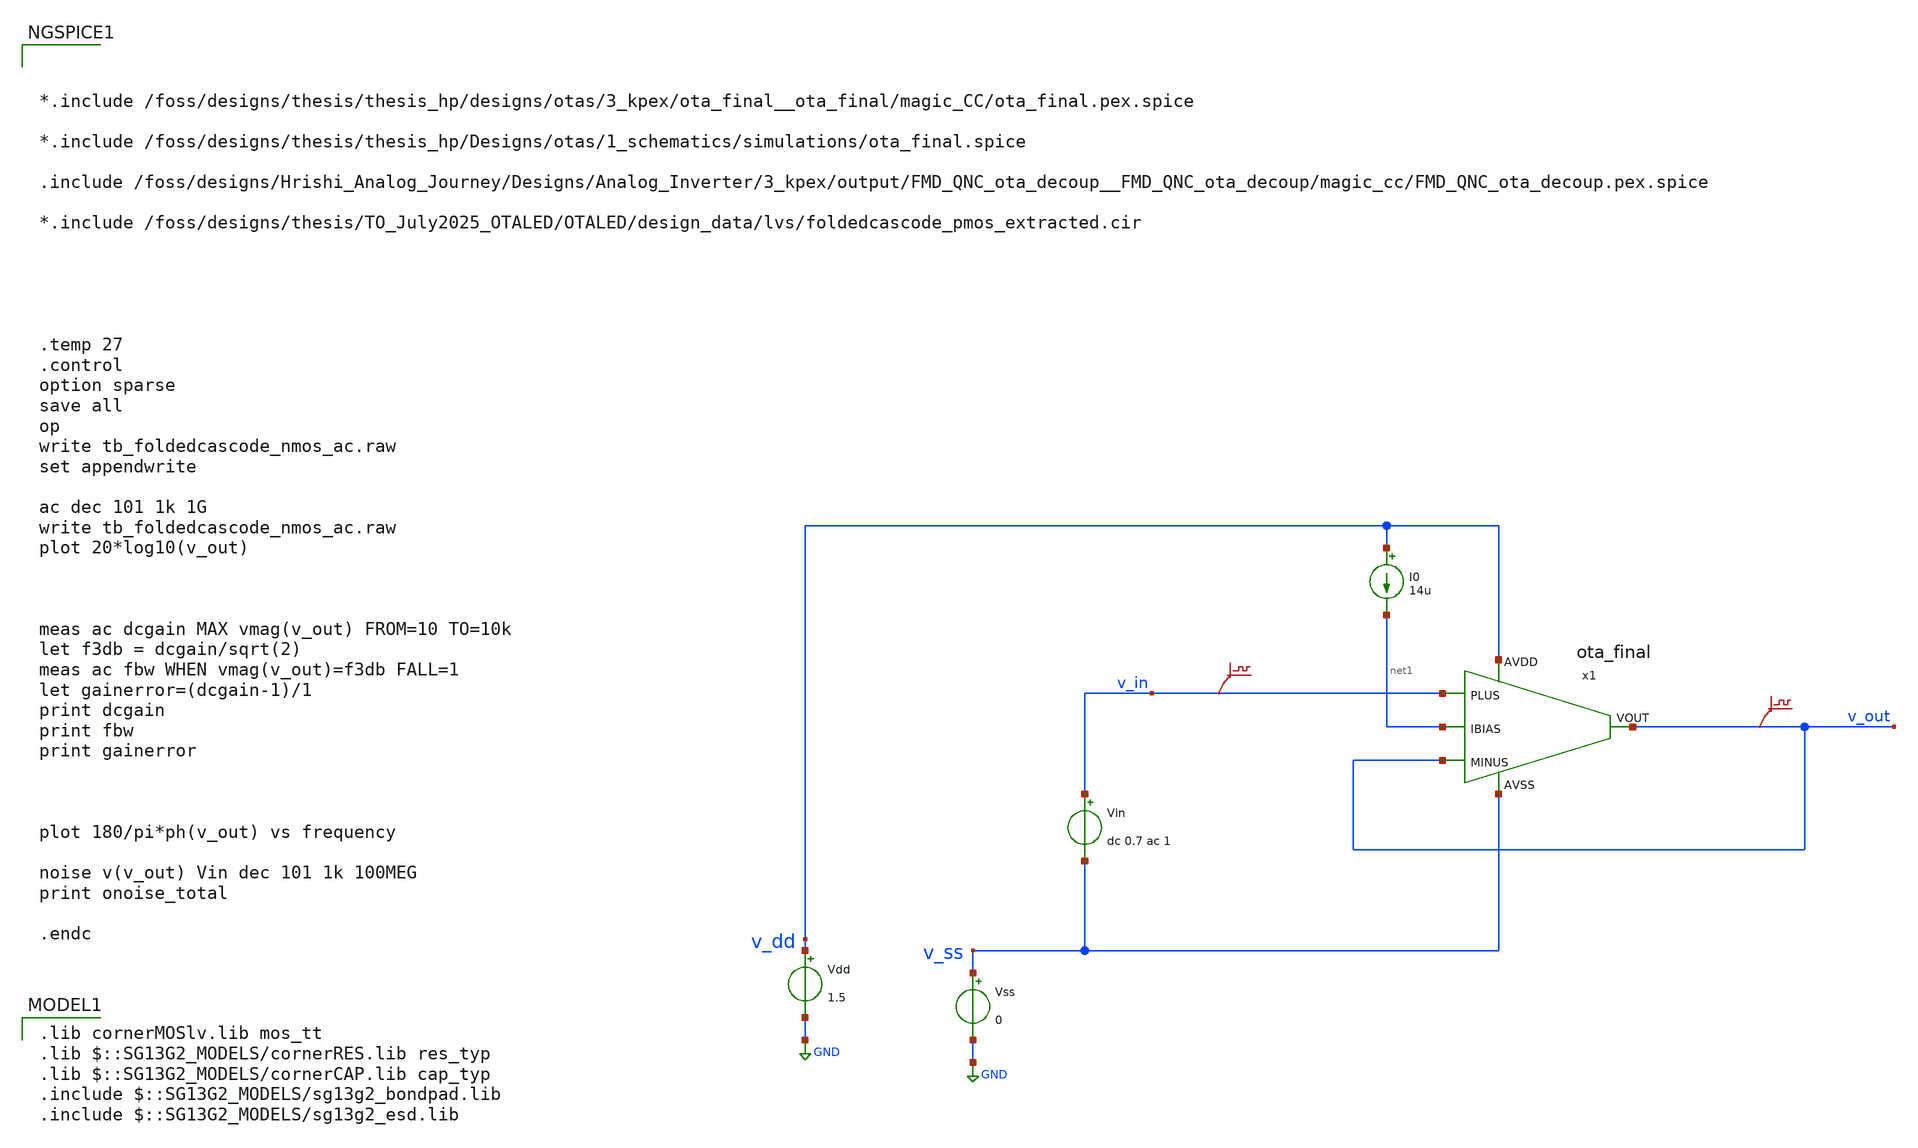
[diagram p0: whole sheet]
** sch_path: Designs/otas/3_kpex/postlayout_testbenches/tb_foldedcascode_nmos_ac.sch
* (c) 2025 Thesis_HP, Apache-2.0 license
**.subckt tb_foldedcascode_nmos_ac
Vss v_ss GND 0
Vdd v_dd GND 1.5
Vin v_in v_ss dc 0.7 ac 1
.save v(v_in)
I0 v_dd net1 14u
.save v(v_out)
x1 v_dd net1 v_out v_out v_in v_ss ota_final
**** begin user architecture code



*.include /foss/designs/thesis/thesis_hp/designs/otas/3_kpex/ota_final__ota_final/magic_CC/ota_final.pex.spice

*.include /foss/designs/thesis/thesis_hp/Designs/otas/1_schematics/simulations/ota_final.spice

.include /foss/designs/Hrishi_Analog_Journey/Designs/Analog_Inverter/3_kpex/output/FMD_QNC_ota_decoup__FMD_QNC_ota_decoup/magic_cc/FMD_QNC_ota_decoup.pex.spice

*.include /foss/designs/thesis/TO_July2025_OTALED/OTALED/design_data/lvs/foldedcascode_pmos_extracted.cir





.temp 27
.control
option sparse
save all
op
write tb_foldedcascode_nmos_ac.raw
set appendwrite

ac dec 101 1k 1G
write tb_foldedcascode_nmos_ac.raw
plot 20*log10(v_out)



meas ac dcgain MAX vmag(v_out) FROM=10 TO=10k
let f3db = dcgain/sqrt(2)
meas ac fbw WHEN vmag(v_out)=f3db FALL=1
let gainerror=(dcgain-1)/1
print dcgain
print fbw
print gainerror



plot 180/pi*ph(v_out) vs frequency

noise v(v_out) Vin dec 101 1k 100MEG
print onoise_total

.endc


 .lib cornerMOSlv.lib mos_tt
.lib $::SG13G2_MODELS/cornerRES.lib res_typ
.lib $::SG13G2_MODELS/cornerCAP.lib cap_typ
.include $::SG13G2_MODELS/sg13g2_bondpad.lib
.include $::SG13G2_MODELS/sg13g2_esd.lib

**** end user architecture code
**.ends
.GLOBAL GND
.end
